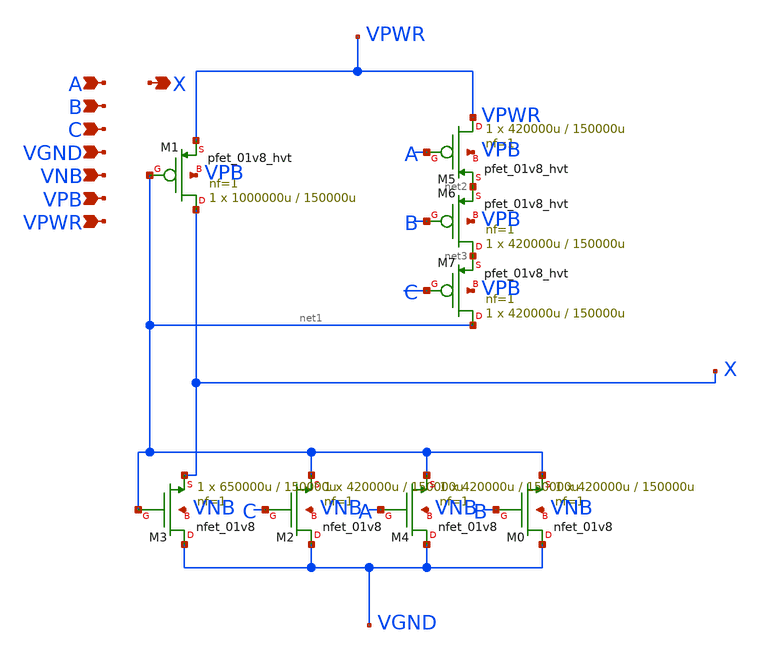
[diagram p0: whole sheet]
** sch_path: schematics/or3/sky130_fd_sc_hd__or3_1.sch
**.subckt sky130_fd_sc_hd__or3_1 A X B VGND VNB VPB VPWR C
*.ipin A
*.opin X
*.ipin B
*.ipin VGND
*.ipin VNB
*.ipin VPB
*.ipin VPWR
*.ipin C
XM0 VGND B net1 VNB sky130_fd_pr__nfet_01v8 L=150000u W=420000u nf=1 ad='int((1 + 1)/2) * 420000u / 1 * 0.29'
+ as='int((1 + 2)/2) * 420000u / 1 * 0.29' pd='2*int((1 + 1)/2) * (420000u / 1 + 0.29)' ps='2*int((1 + 2)/2) * (420000u / 1 + 0.29)'
+ nrd='0.29 / 420000u ' nrs='0.29 / 420000u ' sa=0 sb=0 sd=0 mult=1 m=1
XM1 X net1 VPWR VPB sky130_fd_pr__pfet_01v8_hvt L=150000u W=1000000u nf=1 ad='int((nf+1)/2) * W/nf * 0.29'
+ as='int((nf+2)/2) * W/nf * 0.29' pd='2*int((nf+1)/2) * (W/nf + 0.29)' ps='2*int((nf+2)/2) * (W/nf + 0.29)'
+ nrd='0.29 / W' nrs='0.29 / W' sa=0 sb=0 sd=0 mult=1 m=1
XM2 VGND C net1 VNB sky130_fd_pr__nfet_01v8 L=150000u W=420000u nf=1 ad='int((1 + 1)/2) * 420000u / 1 * 0.29'
+ as='int((1 + 2)/2) * 420000u / 1 * 0.29' pd='2*int((1 + 1)/2) * (420000u / 1 + 0.29)' ps='2*int((1 + 2)/2) * (420000u / 1 + 0.29)'
+ nrd='0.29 / 420000u ' nrs='0.29 / 420000u ' sa=0 sb=0 sd=0 mult=1 m=1
XM5 VPWR A net2 VPB sky130_fd_pr__pfet_01v8_hvt L=150000u W=420000u nf=1 ad='int((nf+1)/2) * W/nf * 0.29'
+ as='int((nf+2)/2) * W/nf * 0.29' pd='2*int((nf+1)/2) * (W/nf + 0.29)' ps='2*int((nf+2)/2) * (W/nf + 0.29)'
+ nrd='0.29 / W' nrs='0.29 / W' sa=0 sb=0 sd=0 mult=1 m=1
XM6 net3 B net2 VPB sky130_fd_pr__pfet_01v8_hvt L=150000u W=420000u nf=1 ad='int((nf+1)/2) * W/nf * 0.29'
+ as='int((nf+2)/2) * W/nf * 0.29' pd='2*int((nf+1)/2) * (W/nf + 0.29)' ps='2*int((nf+2)/2) * (W/nf + 0.29)'
+ nrd='0.29 / W' nrs='0.29 / W' sa=0 sb=0 sd=0 mult=1 m=1
XM7 net1 C net3 VPB sky130_fd_pr__pfet_01v8_hvt L=150000u W=420000u nf=1 ad='int((nf+1)/2) * W/nf * 0.29'
+ as='int((nf+2)/2) * W/nf * 0.29' pd='2*int((nf+1)/2) * (W/nf + 0.29)' ps='2*int((nf+2)/2) * (W/nf + 0.29)'
+ nrd='0.29 / W' nrs='0.29 / W' sa=0 sb=0 sd=0 mult=1 m=1
XM3 VGND net1 X VNB sky130_fd_pr__nfet_01v8 L=150000u W=650000u nf=1 ad='int((1 + 1)/2) * 650000u / 1 * 0.29'
+ as='int((1 + 2)/2) * 650000u / 1 * 0.29' pd='2*int((1 + 1)/2) * (650000u / 1 + 0.29)' ps='2*int((1 + 2)/2) * (650000u / 1 + 0.29)'
+ nrd='0.29 / 650000u ' nrs='0.29 / 650000u ' sa=0 sb=0 sd=0 mult=1 m=1
XM4 VGND A net1 VNB sky130_fd_pr__nfet_01v8 L=150000u W=420000u nf=1 ad='int((1 + 1)/2) * 420000u / 1 * 0.29'
+ as='int((1 + 2)/2) * 420000u / 1 * 0.29' pd='2*int((1 + 1)/2) * (420000u / 1 + 0.29)' ps='2*int((1 + 2)/2) * (420000u / 1 + 0.29)'
+ nrd='0.29 / 420000u ' nrs='0.29 / 420000u ' sa=0 sb=0 sd=0 mult=1 m=1
**.ends
.end
